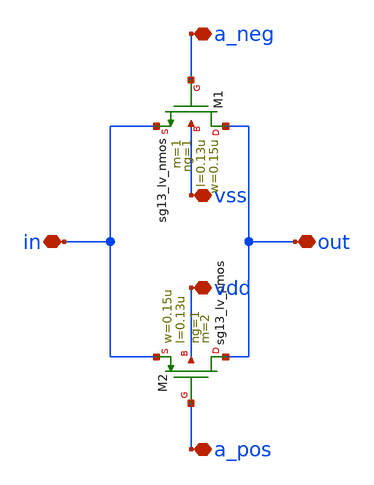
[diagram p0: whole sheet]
** sch_path: design/blocks/transmissiongate/schematic/transmissiongate.sch
**.subckt transmissiongate a_neg a_pos out in vss vdd
*.iopin a_neg
*.iopin a_pos
*.iopin out
*.iopin in
*.iopin vss
*.iopin vdd
XM1 out a_neg in vss sg13_lv_nmos w=0.15u l=0.13u ng=1 m=1 mm_ok=1
XM2 out a_pos in vdd sg13_lv_pmos w=0.15u l=0.13u ng=1 m=2 mm_ok=1
**.ends
.end
